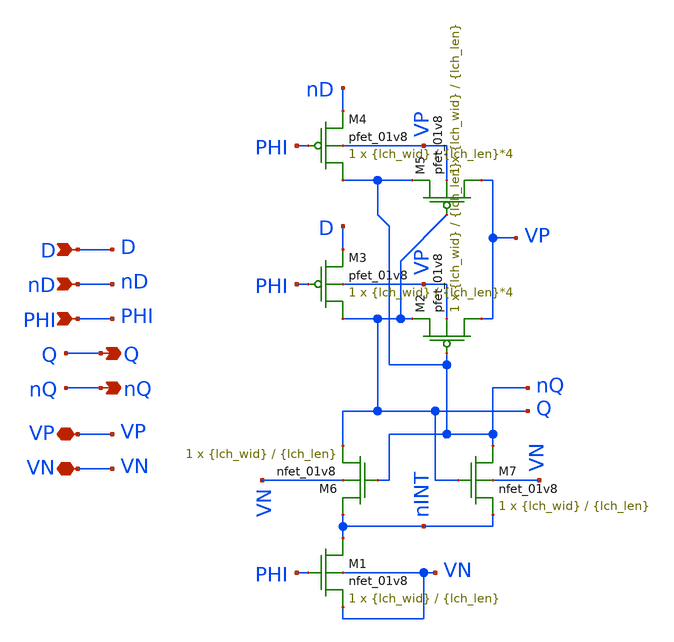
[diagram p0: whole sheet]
** sch_path: n_csrl_latch2.sch
**.subckt n_csrl_latch2 VP D Q nD PHI nQ VN
*.iopin VP
*.ipin D
*.opin Q
*.ipin nD
*.ipin PHI
*.opin nQ
*.iopin VN
XM1 nINT PHI VN VN sky130_fd_pr__nfet_01v8 L={lch_len} W={lch_wid} nf=1 ad='int((nf+1)/2) * W/nf * 0.29'
+ as='int((nf+2)/2) * W/nf * 0.29' pd='2*int((nf+1)/2) * (W/nf + 0.29)' ps='2*int((nf+2)/2) * (W/nf + 0.29)'
+ nrd='0.29 / W' nrs='0.29 / W' sa=0 sb=0 sd=0 mult=1 m=1
XM2 VP nQ Q VP sky130_fd_pr__pfet_01v8 L={lch_len} W={lch_wid} nf=1 ad='int((nf+1)/2) * W/nf * 0.29'
+ as='int((nf+2)/2) * W/nf * 0.29' pd='2*int((nf+1)/2) * (W/nf + 0.29)' ps='2*int((nf+2)/2) * (W/nf + 0.29)'
+ nrd='0.29 / W' nrs='0.29 / W' sa=0 sb=0 sd=0 mult=1 m=1
XM3 Q PHI D VP sky130_fd_pr__pfet_01v8 L={lch_len}*4 W={lch_wid} nf=1 ad='int((nf+1)/2) * W/nf * 0.29'
+ as='int((nf+2)/2) * W/nf * 0.29' pd='2*int((nf+1)/2) * (W/nf + 0.29)' ps='2*int((nf+2)/2) * (W/nf + 0.29)'
+ nrd='0.29 / W' nrs='0.29 / W' sa=0 sb=0 sd=0 mult=1 m=1
XM4 nQ PHI nD VP sky130_fd_pr__pfet_01v8 L={lch_len}*4 W={lch_wid} nf=1 ad='int((nf+1)/2) * W/nf * 0.29'
+ as='int((nf+2)/2) * W/nf * 0.29' pd='2*int((nf+1)/2) * (W/nf + 0.29)' ps='2*int((nf+2)/2) * (W/nf + 0.29)'
+ nrd='0.29 / W' nrs='0.29 / W' sa=0 sb=0 sd=0 mult=1 m=1
XM5 VP Q nQ VP sky130_fd_pr__pfet_01v8 L={lch_len} W={lch_wid} nf=1 ad='int((nf+1)/2) * W/nf * 0.29'
+ as='int((nf+2)/2) * W/nf * 0.29' pd='2*int((nf+1)/2) * (W/nf + 0.29)' ps='2*int((nf+2)/2) * (W/nf + 0.29)'
+ nrd='0.29 / W' nrs='0.29 / W' sa=0 sb=0 sd=0 mult=1 m=1
XM6 nINT nQ Q VN sky130_fd_pr__nfet_01v8 L={lch_len} W={lch_wid} nf=1 ad='int((nf+1)/2) * W/nf * 0.29'
+ as='int((nf+2)/2) * W/nf * 0.29' pd='2*int((nf+1)/2) * (W/nf + 0.29)' ps='2*int((nf+2)/2) * (W/nf + 0.29)'
+ nrd='0.29 / W' nrs='0.29 / W' sa=0 sb=0 sd=0 mult=1 m=1
XM7 nQ Q nINT VN sky130_fd_pr__nfet_01v8 L={lch_len} W={lch_wid} nf=1 ad='int((nf+1)/2) * W/nf * 0.29'
+ as='int((nf+2)/2) * W/nf * 0.29' pd='2*int((nf+1)/2) * (W/nf + 0.29)' ps='2*int((nf+2)/2) * (W/nf + 0.29)'
+ nrd='0.29 / W' nrs='0.29 / W' sa=0 sb=0 sd=0 mult=1 m=1
**.ends
.end
